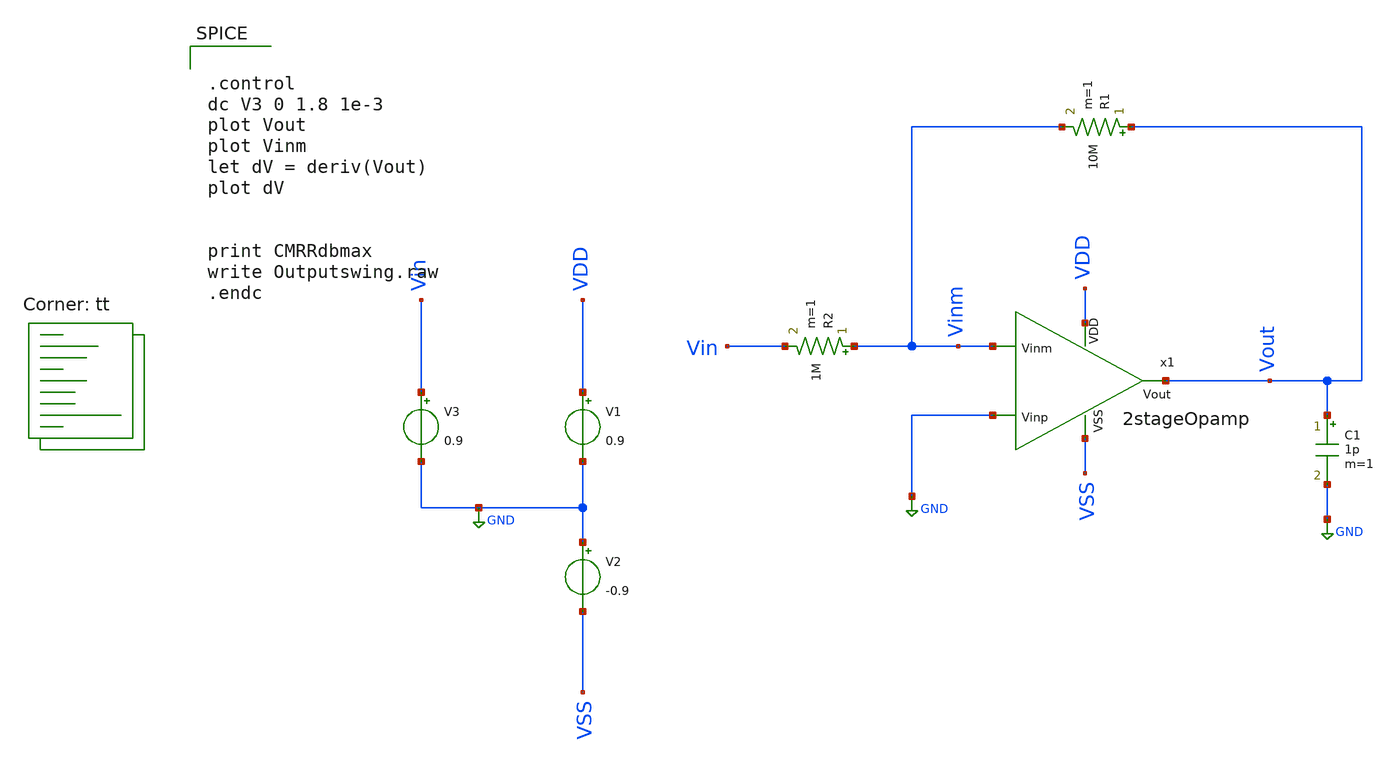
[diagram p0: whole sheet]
** sch_path: TestBenches/Outputswing.sch
**.subckt Outputswing
V1 VDD GND 0.9
V2 GND VSS -0.9
V3 Vin GND 0.9
x1 VDD Vinm GND Vout VSS 2stageOpamp
C1 Vout GND 1p m=1
R1 Vout Vinm 10M m=1
R2 Vinm Vin 1M m=1
**** begin user architecture code


.control
dc V3 0 1.8 1e-3
plot Vout
plot Vinm
let dV = deriv(Vout)
plot dV


print CMRRdbmax
write Outputswing.raw
.endc



.lib $::SKYWATER_MODELS/sky130.lib.spice tt
**** end user architecture code
**.ends
.GLOBAL GND
.end
